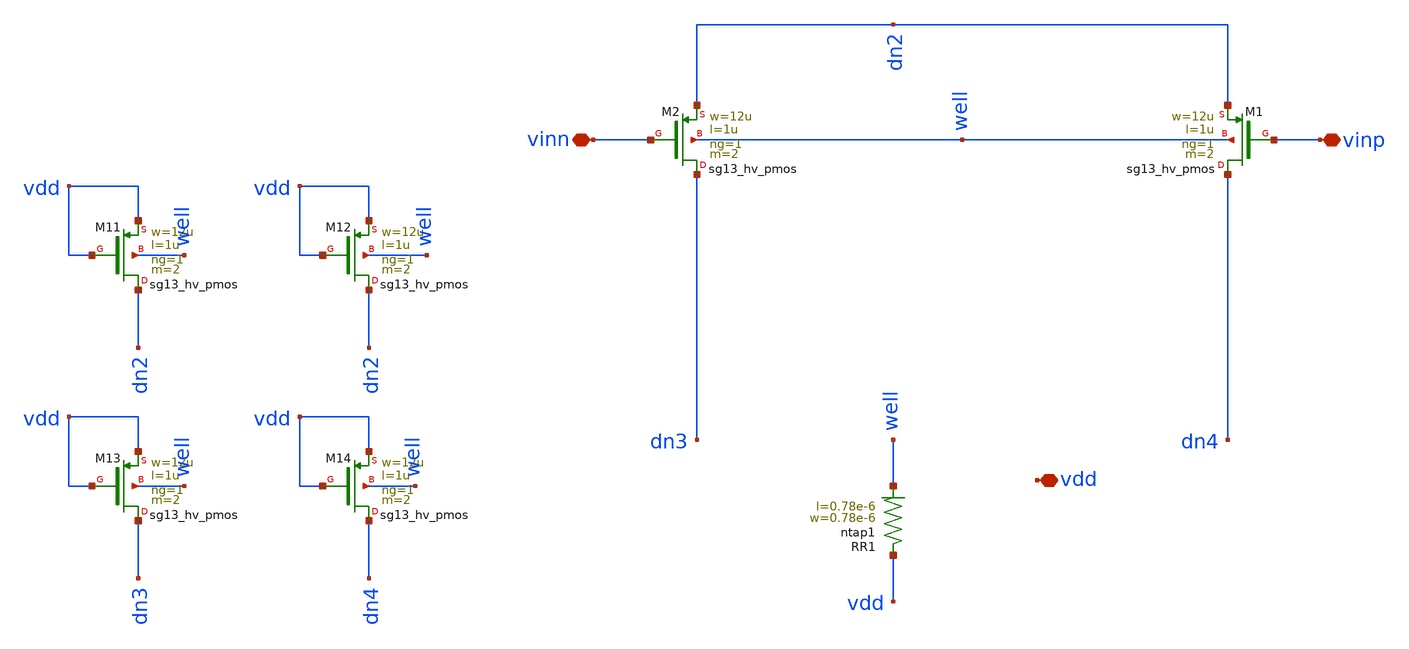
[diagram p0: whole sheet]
** sch_path: dependencies/pmu_ip/dependencies/OTA/OTA-main/schematic/xschem/input_pair.sch
**.subckt input_pair vinp vinn vdd
*.iopin vinp
*.iopin vinn
*.iopin vdd
XM1 dn4 vinp dn2 well sg13_hv_pmos w=12u l=1u ng=1 m=2 mm_ok=1
XM2 dn3 vinn dn2 well sg13_hv_pmos w=12u l=1u ng=1 m=2 mm_ok=1
XM11 dn2 vdd vdd well sg13_hv_pmos w=12u l=1u ng=1 m=2 mm_ok=1
XM12 dn2 vdd vdd well sg13_hv_pmos w=12u l=1u ng=1 m=2 mm_ok=1
XM13 dn3 vdd vdd well sg13_hv_pmos w=12u l=1u ng=1 m=2 mm_ok=1
XM14 dn4 vdd vdd well sg13_hv_pmos w=12u l=1u ng=1 m=2 mm_ok=1
XR1 vdd well ntap1 R=262.8 w=0.78e-6 l=0.78e-6
**.ends
.end
